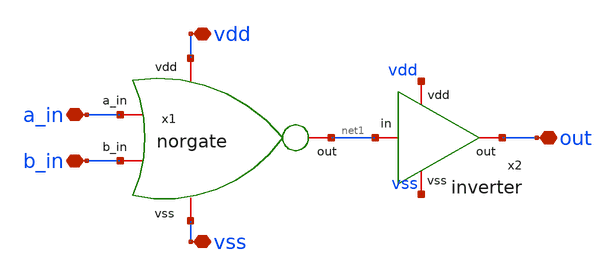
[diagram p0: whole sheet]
** sch_path: design/blocks/xorgate/schematic/orgate.sch
**.subckt orgate a_in b_in out vdd vss
*.iopin a_in
*.iopin b_in
*.iopin out
*.iopin vdd
*.iopin vss
x1 vdd b_in a_in net1 vss norgate
x2 vdd out net1 vss inverter
**.ends

* expanding   symbol:  blocks/norgate/schematic/norgate.sym # of pins=5
** sym_path: blocks/norgate/schematic/norgate.sym
** sch_path: blocks/norgate/schematic/norgate.sch
.subckt norgate vdd b_in a_in out vss
*.iopin vdd
*.iopin vss
*.iopin a_in
*.iopin b_in
*.iopin out
XM1 out a_in vss vss sg13_lv_nmos w=0.15u l=0.13u ng=1 m=1 mm_ok=1
XM2 out b_in vss vss sg13_lv_nmos w=0.15u l=0.13u ng=1 m=1 mm_ok=1
XM3 out b_in net1 vdd sg13_lv_pmos w=0.15u l=0.13u ng=1 m=1 mm_ok=1
XM4 net1 a_in vdd vdd sg13_lv_pmos w=0.15u l=0.13u ng=1 m=1 mm_ok=1
.ends


* expanding   symbol:  blocks/inverter/schematic/inverter.sym # of pins=4
** sym_path: blocks/inverter/schematic/inverter.sym
** sch_path: blocks/inverter/schematic/inverter.sch
.subckt inverter vdd out in vss
*.iopin vdd
*.iopin vss
*.iopin out
*.iopin in
XM2 out in vdd vdd sg13_lv_pmos w=0.3u l=0.13u ng=1 m=1 mm_ok=1
XM1 out in vss vss sg13_lv_nmos w=0.15u l=0.13u ng=1 m=1 mm_ok=1
.ends

.end
